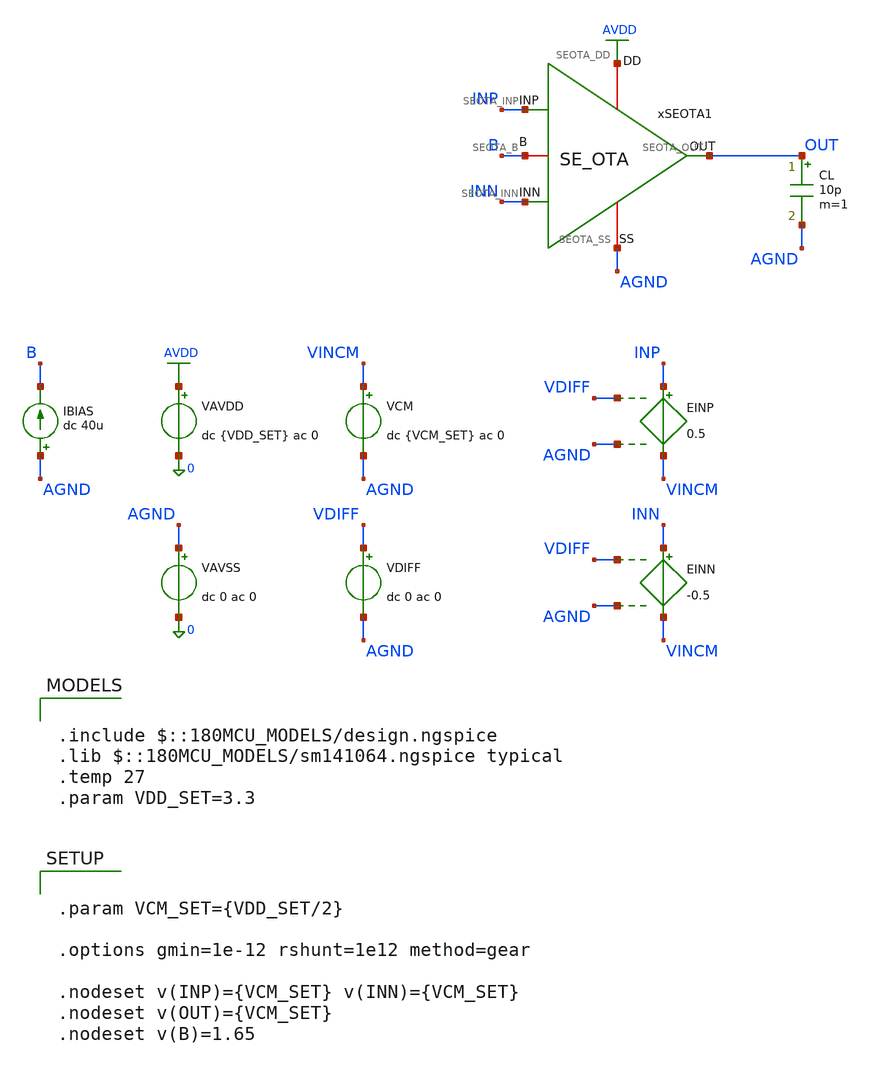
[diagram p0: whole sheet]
** sch_path: Design_Files/IC Design/Testbench/SE_OTA/Open_Loop/SE_OTA_TB_OL_NOM.sch
**.subckt SE_OTA_TB_OL_NOM
IBIAS AGND B dc 40u
VAVDD AVDD 0 dc {VDD_SET} ac 0
.save i(vavdd)
CL OUT AGND 10p m=1
VCM VINCM AGND dc {VCM_SET} ac 0
VDIFF VDIFF AGND dc 0 ac 0
xSEOTA1 AVDD AGND INP INN OUT B SE_OTA
VAVSS AGND 0 dc 0 ac 0
.save i(vavss)
EINN INN VINCM VDIFF AGND -0.5
EINP INP VINCM VDIFF AGND 0.5
**** begin user architecture code

.include $::180MCU_MODELS/design.ngspice
.lib $::180MCU_MODELS/sm141064.ngspice typical
.temp 27
.param VDD_SET=3.3




.control
destroy all
save all
set wr_vecnames
set wr_singlescale
option numdgt=15

shell mkdir -p
+ /foss/designs/ECG_Acquisition_IC/Measurement_Results/IC_Simulation/SE_OTA/NOM.Result_txt

shell rm -f
+ /foss/designs/ECG_Acquisition_IC/Measurement_Results/IC_Simulation/SE_OTA/NOM.Result_txt/NOM.ol_op.txt
shell rm -f
+ /foss/designs/ECG_Acquisition_IC/Measurement_Results/IC_Simulation/SE_OTA/NOM.Result_txt/NOM.ol_diff_ac.txt
shell rm -f
+ /foss/designs/ECG_Acquisition_IC/Measurement_Results/IC_Simulation/SE_OTA/NOM.Result_txt/NOM.ol_cm_ac.txt
shell rm -f
+ /foss/designs/ECG_Acquisition_IC/Measurement_Results/IC_Simulation/SE_OTA/NOM.Result_txt/NOM.ol_psrrp_ac.txt
shell rm -f
+ /foss/designs/ECG_Acquisition_IC/Measurement_Results/IC_Simulation/SE_OTA/NOM.Result_txt/NOM.ol_psrrn_ac.txt
shell rm -f
+ /foss/designs/ECG_Acquisition_IC/Measurement_Results/IC_Simulation/SE_OTA/NOM.Result_txt/NOM.ol_vtc.txt

* OP
op

let vdd = v(AVDD)-v(AGND)
let vinp = v(INP)-v(AGND)
let vinn = v(INN)-v(AGND)
let vout = v(OUT)-v(AGND)
let idd = -vavdd#branch
let ibias = 40u + 0*v(AVDD)

wrdata
+ /foss/designs/ECG_Acquisition_IC/Measurement_Results/IC_Simulation/SE_OTA/NOM.Result_txt/NOM.ol_op.txt vdd vinp vinn vout v(B) idd ibias

* Diff AC
alter @VCM[ACMAG] = 0
alter @VDIFF[ACMAG] = 1
alter @VDIFF[ACPHASE] = 0
alter @VAVDD[ACMAG] = 0
alter @VAVSS[ACMAG] = 0

ac dec 200 0.01 100G

let vin_diff = v(INP)-v(INN)
let vout = v(OUT)-v(AGND)
let vin_diff_real = real(vin_diff)
let vin_diff_imag = imag(vin_diff)
let vout_real = real(vout)
let vout_imag = imag(vout)

setscale frequency

wrdata
+ /foss/designs/ECG_Acquisition_IC/Measurement_Results/IC_Simulation/SE_OTA/NOM.Result_txt/NOM.ol_diff_ac.txt vin_diff_real vin_diff_imag vout_real vout_imag

* CM AC
alter @VCM[ACMAG] = 1
alter @VCM[ACPHASE] = 0
alter @VDIFF[ACMAG] = 0
alter @VAVDD[ACMAG] = 0
alter @VAVSS[ACMAG] = 0

ac dec 200 0.01 100G

let vin_cm = 0.5*(v(INP)+v(INN))-v(AGND)
let vout = v(OUT)-v(AGND)
let vin_cm_real = real(vin_cm)
let vin_cm_imag = imag(vin_cm)
let vout_real = real(vout)
let vout_imag = imag(vout)

setscale frequency

wrdata
+ /foss/designs/ECG_Acquisition_IC/Measurement_Results/IC_Simulation/SE_OTA/NOM.Result_txt/NOM.ol_cm_ac.txt vin_cm_real vin_cm_imag vout_real vout_imag

* PSRR+
alter @VCM[ACMAG] = 0
alter @VDIFF[ACMAG] = 0
alter @VAVDD[ACMAG] = 1
alter @VAVDD[ACPHASE] = 0
alter @VAVSS[ACMAG] = 0

ac dec 200 0.01 100G

let vavdd_ac = v(AVDD)-v(AGND)
let vout = v(OUT)-v(AGND)
let vavdd_real = real(vavdd_ac)
let vavdd_imag = imag(vavdd_ac)
let vout_real = real(vout)
let vout_imag = imag(vout)

setscale frequency

wrdata
+ /foss/designs/ECG_Acquisition_IC/Measurement_Results/IC_Simulation/SE_OTA/NOM.Result_txt/NOM.ol_psrrp_ac.txt vavdd_real vavdd_imag vout_real vout_imag

* PSRR-
alter @VCM[ACMAG] = 0
alter @VDIFF[ACMAG] = 0
alter @VAVDD[ACMAG] = 0
alter @VAVSS[ACMAG] = 1
alter @VAVSS[ACPHASE] = 0

ac dec 200 0.01 100G

let vagnd_ac = v(AGND)
let vout = v(OUT)-v(AGND)
let vagnd_real = real(vagnd_ac)
let vagnd_imag = imag(vagnd_ac)
let vout_real = real(vout)
let vout_imag = imag(vout)

setscale frequency

wrdata
+ /foss/designs/ECG_Acquisition_IC/Measurement_Results/IC_Simulation/SE_OTA/NOM.Result_txt/NOM.ol_psrrn_ac.txt vagnd_real vagnd_imag vout_real vout_imag

* VTC
alter @VCM[ACMAG] = 0
alter @VDIFF[ACMAG] = 0
alter @VAVDD[ACMAG] = 0
alter @VAVSS[ACMAG] = 0

dc VDIFF -20m 20m 1u

let vin_cm = 0.5*(v(INP)+v(INN))-v(AGND)
let vin_diff = v(INP)-v(INN)
let vout = v(OUT)-v(AGND)
let idd = -vavdd#branch

setscale vin_diff

wrdata
+ /foss/designs/ECG_Acquisition_IC/Measurement_Results/IC_Simulation/SE_OTA/NOM.Result_txt/NOM.ol_vtc.txt vin_cm v(INP) v(INN) vout idd

* op
* show m : id vgs vds vth vdsat gm gds
quit
.endc




.param VCM_SET={VDD_SET/2}

.options gmin=1e-12 rshunt=1e12 method=gear

.nodeset v(INP)={VCM_SET} v(INN)={VCM_SET}
.nodeset v(OUT)={VCM_SET}
.nodeset v(B)=1.65


**** end user architecture code
**.ends

* expanding   symbol:  ECG_Acquisition_IC/Design_Files/IC Design/Schematic/SE_OTA/SE_OTA.sym # of
*+ pins=6
** sym_path: Design_Files/IC Design/Schematic/SE_OTA/SE_OTA.sym
** sch_path: Design_Files/IC Design/Schematic/SE_OTA/SE_OTA.sch
.subckt SE_OTA SEOTA_DD SEOTA_SS SEOTA_INP SEOTA_INN SEOTA_OUT SEOTA_B
*.iopin SEOTA_DD
*.iopin SEOTA_SS
*.ipin SEOTA_INP
*.ipin SEOTA_INN
*.opin SEOTA_OUT
*.iopin SEOTA_B
XM3 net4 net4 SEOTA_DD SEOTA_DD pfet_03v3 L=4u W=1u nf=1 ad='int((nf+1)/2) * W/nf * 0.18u' as='int((nf+2)/2) * W/nf * 0.18u'
+ pd='2*int((nf+1)/2) * (W/nf + 0.18u)' ps='2*int((nf+2)/2) * (W/nf + 0.18u)' nrd='0.18u / W' nrs='0.18u / W'
+ sa=0 sb=0 sd=0 m=60
XM7 SEOTA_OUT SEOTA_B SEOTA_SS SEOTA_SS nfet_03v3 L=0.5u W=1u nf=1 ad='int((nf+1)/2) * W/nf * 0.18u'
+ as='int((nf+2)/2) * W/nf * 0.18u' pd='2*int((nf+1)/2) * (W/nf + 0.18u)' ps='2*int((nf+2)/2) * (W/nf + 0.18u)'
+ nrd='0.18u / W' nrs='0.18u / W' sa=0 sb=0 sd=0 m=100
Rz net1 net2 3.8k m=1
XM5 net3 SEOTA_B SEOTA_SS SEOTA_SS nfet_03v3 L=2u W=1u nf=1 ad='int((nf+1)/2) * W/nf * 0.18u' as='int((nf+2)/2) * W/nf * 0.18u'
+ pd='2*int((nf+1)/2) * (W/nf + 0.18u)' ps='2*int((nf+2)/2) * (W/nf + 0.18u)' nrd='0.18u / W' nrs='0.18u / W'
+ sa=0 sb=0 sd=0 m=10
XM6 SEOTA_OUT net1 SEOTA_DD SEOTA_DD pfet_03v3 L=0.5u W=1u nf=1 ad='int((nf+1)/2) * W/nf * 0.18u' as='int((nf+2)/2) * W/nf * 0.18u'
+ pd='2*int((nf+1)/2) * (W/nf + 0.18u)' ps='2*int((nf+2)/2) * (W/nf + 0.18u)' nrd='0.18u / W' nrs='0.18u / W'
+ sa=0 sb=0 sd=0 m=400
XM8 SEOTA_B SEOTA_B SEOTA_SS SEOTA_SS nfet_03v3 L=2u W=1u nf=1 ad='int((nf+1)/2) * W/nf * 0.18u' as='int((nf+2)/2) * W/nf * 0.18u'
+ pd='2*int((nf+1)/2) * (W/nf + 0.18u)' ps='2*int((nf+2)/2) * (W/nf + 0.18u)' nrd='0.18u / W' nrs='0.18u / W'
+ sa=0 sb=0 sd=0 m=20
Cc net2 SEOTA_OUT 2p m=1
XM4 net1 net4 SEOTA_DD SEOTA_DD pfet_03v3 L=4u W=1u nf=1 ad='int((nf+1)/2) * W/nf * 0.18u' as='int((nf+2)/2) * W/nf * 0.18u'
+ pd='2*int((nf+1)/2) * (W/nf + 0.18u)' ps='2*int((nf+2)/2) * (W/nf + 0.18u)' nrd='0.18u / W' nrs='0.18u / W'
+ sa=0 sb=0 sd=0 m=60
XM1 net4 SEOTA_INN net3 SEOTA_SS nfet_03v3 L=4u W=1u nf=1 ad='int((nf+1)/2) * W/nf * 0.18u' as='int((nf+2)/2) * W/nf * 0.18u'
+ pd='2*int((nf+1)/2) * (W/nf + 0.18u)' ps='2*int((nf+2)/2) * (W/nf + 0.18u)' nrd='0.18u / W' nrs='0.18u / W'
+ sa=0 sb=0 sd=0 m=400
XM2 net1 SEOTA_INP net3 SEOTA_SS nfet_03v3 L=4u W=1u nf=1 ad='int((nf+1)/2) * W/nf * 0.18u' as='int((nf+2)/2) * W/nf * 0.18u'
+ pd='2*int((nf+1)/2) * (W/nf + 0.18u)' ps='2*int((nf+2)/2) * (W/nf + 0.18u)' nrd='0.18u / W' nrs='0.18u / W'
+ sa=0 sb=0 sd=0 m=400
.ends

.GLOBAL AVDD
.end
